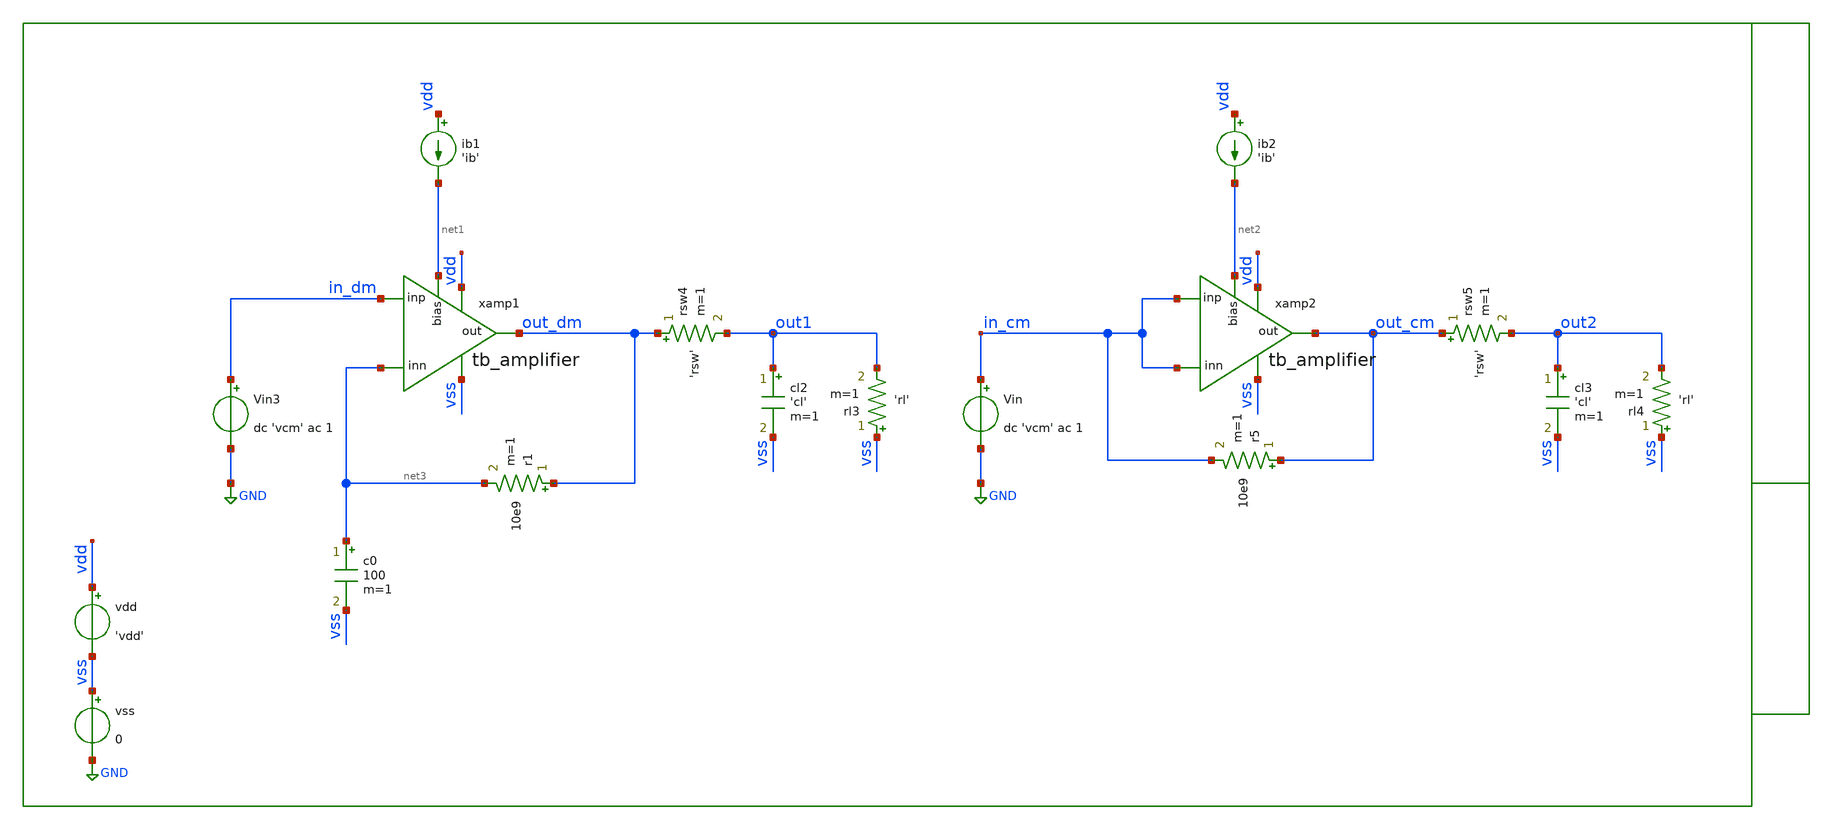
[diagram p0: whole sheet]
** sch_path: xschem/tb/testbuffer/tb_amplifier/ac_tb_amplifier_cmrr.sch
**.subckt ac_tb_amplifier_cmrr
vdd vdd vss 'vdd'
vss vss GND 0
cl2 out1 vss 'cl' m=1
ib1 vdd net1 'ib'
rl3 vss out1 'rl' m=1
xamp1 vdd out_dm in_dm net3 vss net1 tb_amplifier
rsw4 out_dm out1 'rsw' m=1
cl3 out2 vss 'cl' m=1
ib2 vdd net2 'ib'
rl4 vss out2 'rl' m=1
xamp2 vdd out_cm in_cm in_cm vss net2 tb_amplifier
rsw5 out_cm out2 'rsw' m=1
Vin in_cm GND dc 'vcm' ac 1
Vin3 in_dm GND dc 'vcm' ac 1
c0 net3 vss 100 m=1
r1 out_dm net3 10e9 m=1
r5 out_cm in_cm 10e9 m=1
**** begin user architecture code
 * Control

.param vdd=3.3
.param vcm='vdd/2'
.param ib=5u
.param cl=10p
.param rl=1e6
.param rsw=1
.param vin='vcm'

.control
save all
ac dec 10 0.1 1e9
let cmrr_f=(out_dm/out_cm)
meas ac cmrr find vdb(cmrr_f) at=0.1
print cmrr
.endc

 * Model Corners

.include $::CORNERS/ngspice/tt.spice
*.include $::CORNERS/ngspice/ff.spice
*.include $::CORNERS/ngspice/ss.spice
*.include $::CORNERS/ngspice/sf.spice
*.include $::CORNERS/ngspice/fs.spice

**** end user architecture code
**.ends

* expanding   symbol:  sch/testbuffer/tb_amplifier/tb_amplifier.sym # of pins=6
** sym_path: xschem/sch/testbuffer/tb_amplifier/tb_amplifier.sym
** sch_path: xschem/sch/testbuffer/tb_amplifier/tb_amplifier.sch
.subckt tb_amplifier vdd out inp inn vss bias
*.ipin inn
*.ipin inp
*.opin out
*.iopin bias
*.iopin vdd
*.iopin vss
XM3 mirr mirr vdd vdd pfet_06v0 L=4u W=16u nf=2 ad='int((nf+1)/2) * W/nf * 0.18u' as='int((nf+2)/2) * W/nf * 0.18u'
+ pd='2*int((nf+1)/2) * (W/nf + 0.18u)' ps='2*int((nf+2)/2) * (W/nf + 0.18u)' nrd='0.18u / W' nrs='0.18u / W'
+ sa=0 sb=0 sd=0 m=2 par=2
XM4 comp mirr vdd vdd pfet_06v0 L=4u W=16u nf=2 ad='int((nf+1)/2) * W/nf * 0.18u' as='int((nf+2)/2) * W/nf * 0.18u'
+ pd='2*int((nf+1)/2) * (W/nf + 0.18u)' ps='2*int((nf+2)/2) * (W/nf + 0.18u)' nrd='0.18u / W' nrs='0.18u / W'
+ sa=0 sb=0 sd=0 m=2 par=2
XM2 comp inp vcm vss nfet_06v0 L=2u W=16u nf=2 ad='int((nf+1)/2) * W/nf * 0.18u' as='int((nf+2)/2) * W/nf * 0.18u'
+ pd='2*int((nf+1)/2) * (W/nf + 0.18u)' ps='2*int((nf+2)/2) * (W/nf + 0.18u)' nrd='0.18u / W' nrs='0.18u / W'
+ sa=0 sb=0 sd=0 m=2 par=2
XM1 mirr inn vcm vss nfet_06v0 L=2u W=16u nf=2 ad='int((nf+1)/2) * W/nf * 0.18u' as='int((nf+2)/2) * W/nf * 0.18u'
+ pd='2*int((nf+1)/2) * (W/nf + 0.18u)' ps='2*int((nf+2)/2) * (W/nf + 0.18u)' nrd='0.18u / W' nrs='0.18u / W'
+ sa=0 sb=0 sd=0 m=2 par=2
XM5 vcm bias vss vss nfet_06v0 L=1u W=16u nf=2 ad='int((nf+1)/2) * W/nf * 0.18u' as='int((nf+2)/2) * W/nf * 0.18u'
+ pd='2*int((nf+1)/2) * (W/nf + 0.18u)' ps='2*int((nf+2)/2) * (W/nf + 0.18u)' nrd='0.18u / W' nrs='0.18u / W'
+ sa=0 sb=0 sd=0 m=2 par=2
XM6 out bias vss vss nfet_06v0 L=1u W=16u nf=2 ad='int((nf+1)/2) * W/nf * 0.18u' as='int((nf+2)/2) * W/nf * 0.18u'
+ pd='2*int((nf+1)/2) * (W/nf + 0.18u)' ps='2*int((nf+2)/2) * (W/nf + 0.18u)' nrd='0.18u / W' nrs='0.18u / W'
+ sa=0 sb=0 sd=0 m=12 par=12
XM7 out comp vdd vdd pfet_06v0 L=1u W=96u nf=12 ad='int((nf+1)/2) * W/nf * 0.18u' as='int((nf+2)/2) * W/nf * 0.18u'
+ pd='2*int((nf+1)/2) * (W/nf + 0.18u)' ps='2*int((nf+2)/2) * (W/nf + 0.18u)' nrd='0.18u / W' nrs='0.18u / W'
+ sa=0 sb=0 sd=0 m=1 par=1
XMB1 bias bias vss vss nfet_06v0 L=1u W=16u nf=2 ad='int((nf+1)/2) * W/nf * 0.18u' as='int((nf+2)/2) * W/nf * 0.18u'
+ pd='2*int((nf+1)/2) * (W/nf + 0.18u)' ps='2*int((nf+2)/2) * (W/nf + 0.18u)' nrd='0.18u / W' nrs='0.18u / W'
+ sa=0 sb=0 sd=0 m=2 par=2
XMB2 vbm bias vss vss nfet_06v0 L=1u W=16u nf=2 ad='int((nf+1)/2) * W/nf * 0.18u' as='int((nf+2)/2) * W/nf * 0.18u'
+ pd='2*int((nf+1)/2) * (W/nf + 0.18u)' ps='2*int((nf+2)/2) * (W/nf + 0.18u)' nrd='0.18u / W' nrs='0.18u / W'
+ sa=0 sb=0 sd=0 m=2 par=2
XMB3 vbm vbm vbt vdd pfet_06v0 L=1u W=16u nf=2 ad='int((nf+1)/2) * W/nf * 0.18u' as='int((nf+2)/2) * W/nf * 0.18u'
+ pd='2*int((nf+1)/2) * (W/nf + 0.18u)' ps='2*int((nf+2)/2) * (W/nf + 0.18u)' nrd='0.18u / W' nrs='0.18u / W'
+ sa=0 sb=0 sd=0 m=1 par=1
XMB4 vbt vbt vdd vdd pfet_06v0 L=1u W=16u nf=2 ad='int((nf+1)/2) * W/nf * 0.18u' as='int((nf+2)/2) * W/nf * 0.18u'
+ pd='2*int((nf+1)/2) * (W/nf + 0.18u)' ps='2*int((nf+2)/2) * (W/nf + 0.18u)' nrd='0.18u / W' nrs='0.18u / W'
+ sa=0 sb=0 sd=0 m=1 par=1
XRCC gc comp vdd ppolyf_u_1k_6p0 r_width=2e-6 r_length=38e-6 s=1 m=1
XMDUM1 vss vss vss vss nfet_06v0 L=2u W=16u nf=2 ad='int((nf+1)/2) * W/nf * 0.18u' as='int((nf+2)/2) * W/nf * 0.18u'
+ pd='2*int((nf+1)/2) * (W/nf + 0.18u)' ps='2*int((nf+2)/2) * (W/nf + 0.18u)' nrd='0.18u / W' nrs='0.18u / W'
+ sa=0 sb=0 sd=0 m=2 par=2
XMDUM2 vdd vdd vdd vdd pfet_06v0 L=4u W=16u nf=2 ad='int((nf+1)/2) * W/nf * 0.18u' as='int((nf+2)/2) * W/nf * 0.18u'
+ pd='2*int((nf+1)/2) * (W/nf + 0.18u)' ps='2*int((nf+2)/2) * (W/nf + 0.18u)' nrd='0.18u / W' nrs='0.18u / W'
+ sa=0 sb=0 sd=0 m=4 par=4
XC1 out gc cap_mim_2f0_m4m5_noshield c_width=30e-6 c_length=30e-6 m=1
.ends

.GLOBAL GND
.end
